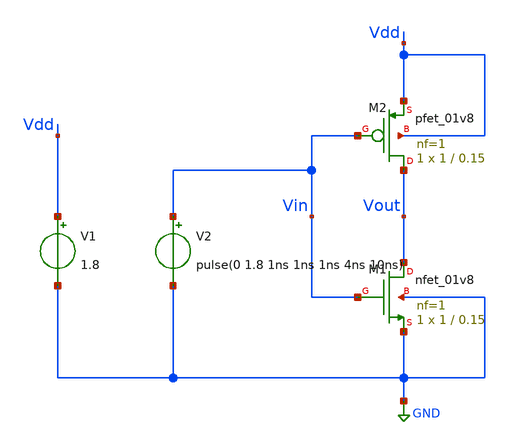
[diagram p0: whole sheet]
** sch_path: TT/inverter_tb.sch
.lib $::SKYWATER_MODELS/sky130.lib.spice tt
.include $::SKYWATER_STDCELLS/sky130_fd_sc_hd.spice

**.subckt inverter_tb
XM1 Vout Vin GND GND sky130_fd_pr__nfet_01v8 L=0.15 W=1 nf=1 ad='int((nf+1)/2) * W/nf * 0.29' as='int((nf+2)/2) * W/nf * 0.29'
+ pd='2*int((nf+1)/2) * (W/nf + 0.29)' ps='2*int((nf+2)/2) * (W/nf + 0.29)' nrd='0.29 / W' nrs='0.29 / W'
+ sa=0 sb=0 sd=0 mult=1 m=1
XM2 Vout Vin Vdd Vdd sky130_fd_pr__pfet_01v8 L=0.15 W=1 nf=1 ad='int((nf+1)/2) * W/nf * 0.29' as='int((nf+2)/2) * W/nf * 0.29'
+ pd='2*int((nf+1)/2) * (W/nf + 0.29)' ps='2*int((nf+2)/2) * (W/nf + 0.29)' nrd='0.29 / W' nrs='0.29 / W'
+ sa=0 sb=0 sd=0 mult=1 m=1
V1 Vdd GND 1.8
V2 Vin GND pulse(0 1.8 1ns 1ns 1ns 4ns 10ns)
**** begin user architecture code


.tran 0.1n 50n
.save all



**** end user architecture code
**.ends
.GLOBAL GND
.end
